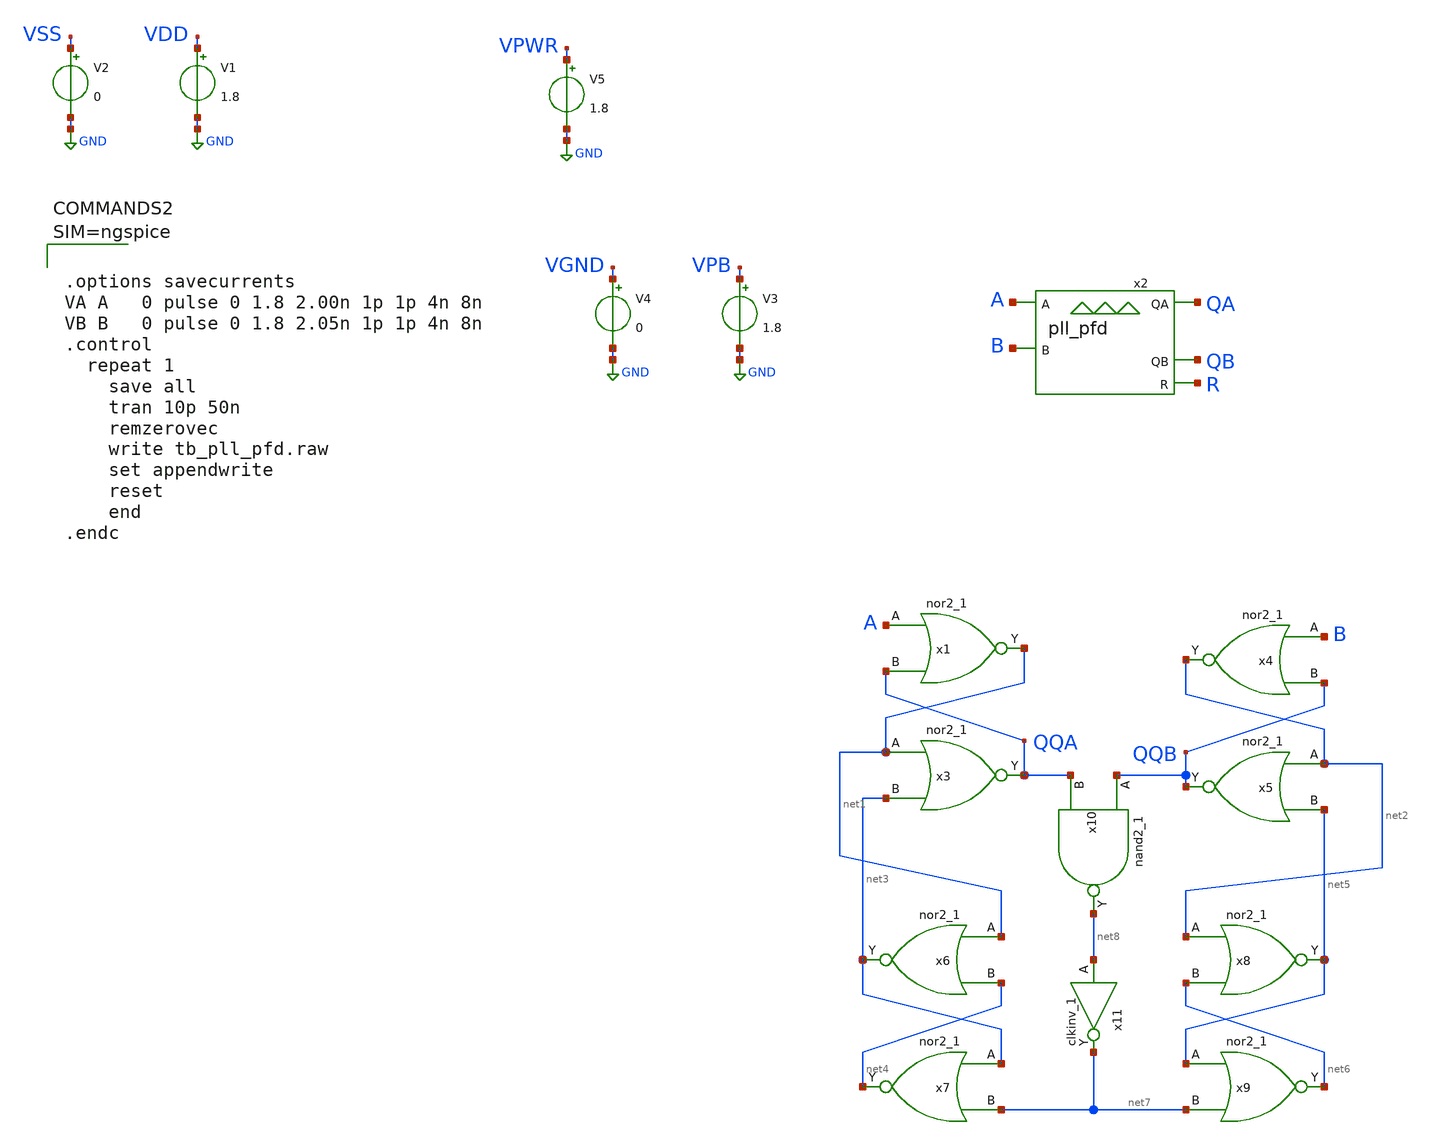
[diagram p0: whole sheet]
** sch_path: xschem/tb_pll_pfd.sch
**.subckt tb_pll_pfd
V1 VDD GND 1.8
V2 VSS GND 0
V5 VPWR GND 1.8
x2 A B QA QB R VDD VSS pll_pfd
x1 A QQA VGND VNB VPB VPWR net1 sky130_fd_sc_hd__nor2_1
x3 net1 net3 VGND VNB VPB VPWR QQA sky130_fd_sc_hd__nor2_1
V3 VPB GND 1.8
V4 VGND GND 0
x4 B QQB VGND VNB VPB VPWR net2 sky130_fd_sc_hd__nor2_1
x5 net2 net5 VGND VNB VPB VPWR QQB sky130_fd_sc_hd__nor2_1
x6 net1 net4 VGND VNB VPB VPWR net3 sky130_fd_sc_hd__nor2_1
x7 net3 net7 VGND VNB VPB VPWR net4 sky130_fd_sc_hd__nor2_1
x8 net2 net6 VGND VNB VPB VPWR net5 sky130_fd_sc_hd__nor2_1
x9 net5 net7 VGND VNB VPB VPWR net6 sky130_fd_sc_hd__nor2_1
x10 QQB QQA VGND VNB VPB VPWR net8 sky130_fd_sc_hd__nand2_1
x11 net8 VGND VNB VPB VPWR net7 sky130_fd_sc_hd__clkinv_1
**** begin user architecture code

** opencircuitdesign pdks install
.lib $::SKYWATER_MODELS/sky130.lib.spice tt_mm
.include $::SKYWATER_STDCELLS/sky130_fd_sc_hd.spice





.options savecurrents
VA A   0 pulse 0 1.8 2.00n 1p 1p 4n 8n
VB B   0 pulse 0 1.8 2.05n 1p 1p 4n 8n
.control
  repeat 1
    save all
    tran 10p 50n
    remzerovec
    write tb_pll_pfd.raw
    set appendwrite
    reset
    end
.endc



**** end user architecture code
**.ends
.GLOBAL GND
.end
